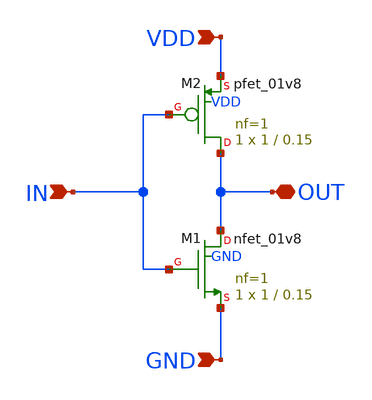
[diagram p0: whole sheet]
** sch_path: design_data/xschem/inv_la.sch
**.subckt inv_la OUT GND VDD IN
*.iopin OUT
*.ipin GND
*.ipin VDD
*.ipin IN
XM1 OUT IN GND GND sky130_fd_pr__nfet_01v8 L=0.15 W=1 nf=1 ad='int((1 + 1)/2) * 1 / 1 * 0.29' as='int((1 + 2)/2) * 1 / 1 * 0.29'
+ pd='2*int((1 + 1)/2) * (1 / 1 + 0.29)' ps='2*int((1 + 2)/2) * (1 / 1 + 0.29)' nrd='0.29 / 1 ' nrs='0.29 / 1 '
+ sa=0 sb=0 sd=0 mult=1 m=1
XM2 OUT IN VDD VDD sky130_fd_pr__pfet_01v8 L=0.15 W=1 nf=1 ad='int((1 + 1)/2) * 1 / 1 * 0.29' as='int((1 + 2)/2) * 1 / 1 * 0.29'
+ pd='2*int((1 + 1)/2) * (1 / 1 + 0.29)' ps='2*int((1 + 2)/2) * (1 / 1 + 0.29)' nrd='0.29 / 1 ' nrs='0.29 / 1 '
+ sa=0 sb=0 sd=0 mult=1 m=1
**.ends
.end
